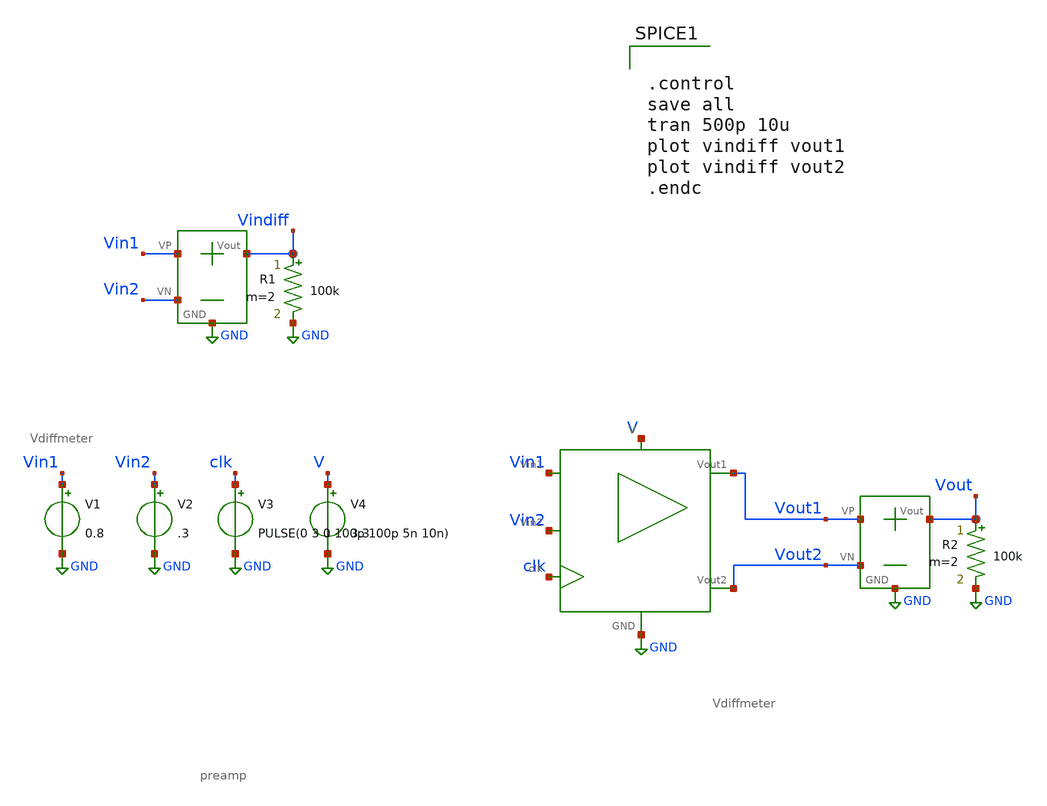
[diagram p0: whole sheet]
** sch_path: SAR_ADC/xschem/test/preamp_tb/untitled.sch
**.subckt untitled
V1 Vin1 GND 0.8
V2 Vin2 GND .3
V3 clk GND PULSE(0 3 0 100p 100p 5n 10n)
V4 V GND 3.3
X2 Vin1 Vin2 Vindiff GND Vdiffmeter
R1 Vindiff GND 100k m=2
X1 V GND Vin1 clk Vout1 Vout2 Vin2 preamp
X3 Vout1 Vout2 Vout GND Vdiffmeter
R2 Vout GND 100k m=2
**** begin user architecture code


.control
save all
tran 500p 10u
plot vindiff vout1
plot vindiff vout2
.endc


.include /foss/pdks/gf180mcuC/libs.tech/ngspice/design.ngspice
.lib /foss/pdks/gf180mcuC/libs.tech/ngspice/sm141064.ngspice typical

**** end user architecture code
**.ends
.GLOBAL GND
.end
